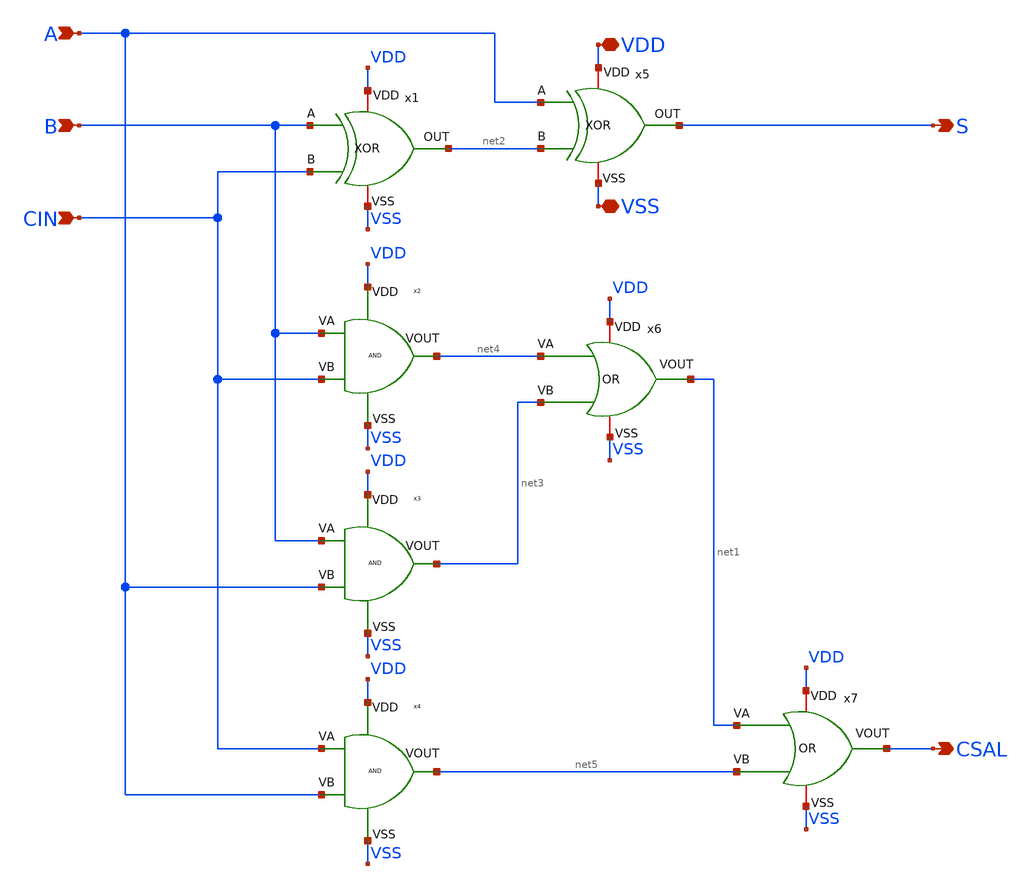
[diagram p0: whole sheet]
** sch_path: ADC8711-main/schematic/xschem/FA.sch
**.subckt FA B A CIN S CSAL VDD VSS
*.ipin B
*.ipin A
*.ipin CIN
*.opin S
*.opin CSAL
*.iopin VDD
*.iopin VSS
x1 net2 B VDD CIN VSS XOR
x5 S A VDD net2 VSS XOR
x6 VDD net1 net4 net3 VSS OR
x7 VDD CSAL net1 net5 VSS OR
x2 VDD B net4 CIN VSS AND
x3 VDD B net3 A VSS AND
x4 VDD CIN net5 A VSS AND
**.ends
.end
